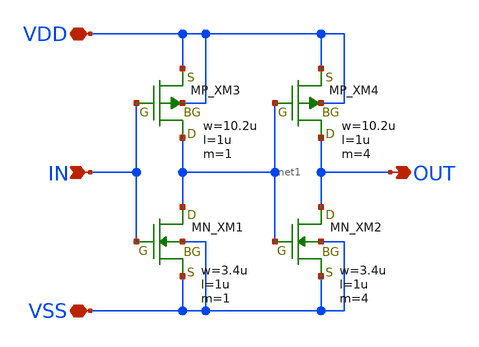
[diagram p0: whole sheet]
** sch_path: member_project/imager/YuMaehashi/design/vsc_bufx1x4.sch
**.subckt vsc_bufx1x4 IN VDD VSS OUT
*.ipin IN
*.iopin VDD
*.iopin VSS
*.opin OUT
XXM1 net1 IN VSS VSS NMOS w=3.4u l=1u nrd=0 nrs=0 m=1
XXM2 OUT net1 VSS VSS NMOS w=3.4u l=1u nrd=0 nrs=0 m=4
XXM3 net1 IN VDD VDD PMOS w=10.2u l=1u nrd=0 nrs=0 m=1
XXM4 OUT net1 VDD VDD PMOS w=10.2u l=1u nrd=0 nrs=0 m=4
**.ends
.end
